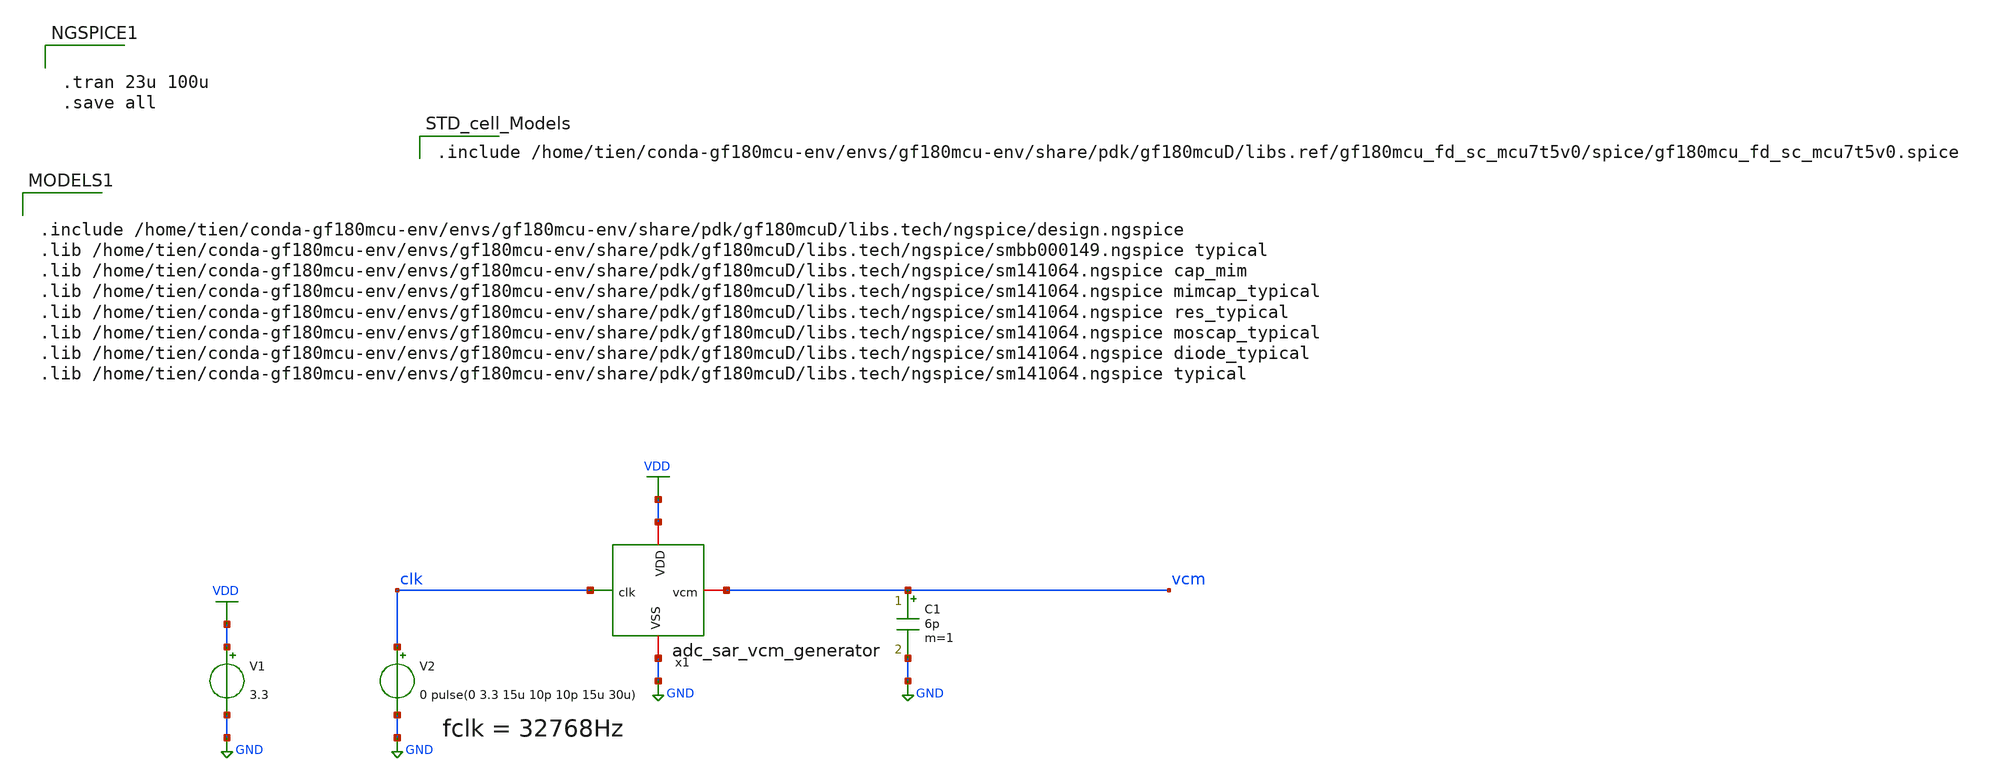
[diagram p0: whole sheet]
** sch_path: spice/adc_sar_vcm_generator_tb.sch
**.subckt adc_sar_vcm_generator_tb
V1 VDD GND 3.3
V2 clk GND 0 pulse(0 3.3 15u 10p 10p 15u 30u)
x1 VDD vcm clk GND adc_sar_vcm_generator
C1 vcm GND 6p m=1
**** begin user architecture code


.tran 23u 100u
.save all



.include /home/tien/conda-gf180mcu-env/envs/gf180mcu-env/share/pdk/gf180mcuD/libs.tech/ngspice/design.ngspice
.lib /home/tien/conda-gf180mcu-env/envs/gf180mcu-env/share/pdk/gf180mcuD/libs.tech/ngspice/smbb000149.ngspice typical
.lib /home/tien/conda-gf180mcu-env/envs/gf180mcu-env/share/pdk/gf180mcuD/libs.tech/ngspice/sm141064.ngspice cap_mim
.lib /home/tien/conda-gf180mcu-env/envs/gf180mcu-env/share/pdk/gf180mcuD/libs.tech/ngspice/sm141064.ngspice mimcap_typical
.lib /home/tien/conda-gf180mcu-env/envs/gf180mcu-env/share/pdk/gf180mcuD/libs.tech/ngspice/sm141064.ngspice res_typical
.lib /home/tien/conda-gf180mcu-env/envs/gf180mcu-env/share/pdk/gf180mcuD/libs.tech/ngspice/sm141064.ngspice moscap_typical
.lib /home/tien/conda-gf180mcu-env/envs/gf180mcu-env/share/pdk/gf180mcuD/libs.tech/ngspice/sm141064.ngspice diode_typical
.lib /home/tien/conda-gf180mcu-env/envs/gf180mcu-env/share/pdk/gf180mcuD/libs.tech/ngspice/sm141064.ngspice typical


.include /home/tien/conda-gf180mcu-env/envs/gf180mcu-env/share/pdk/gf180mcuD/libs.ref/gf180mcu_fd_sc_mcu7t5v0/spice/gf180mcu_fd_sc_mcu7t5v0.spice

**** end user architecture code
**.ends
.GLOBAL GND
.GLOBAL VDD
.end
